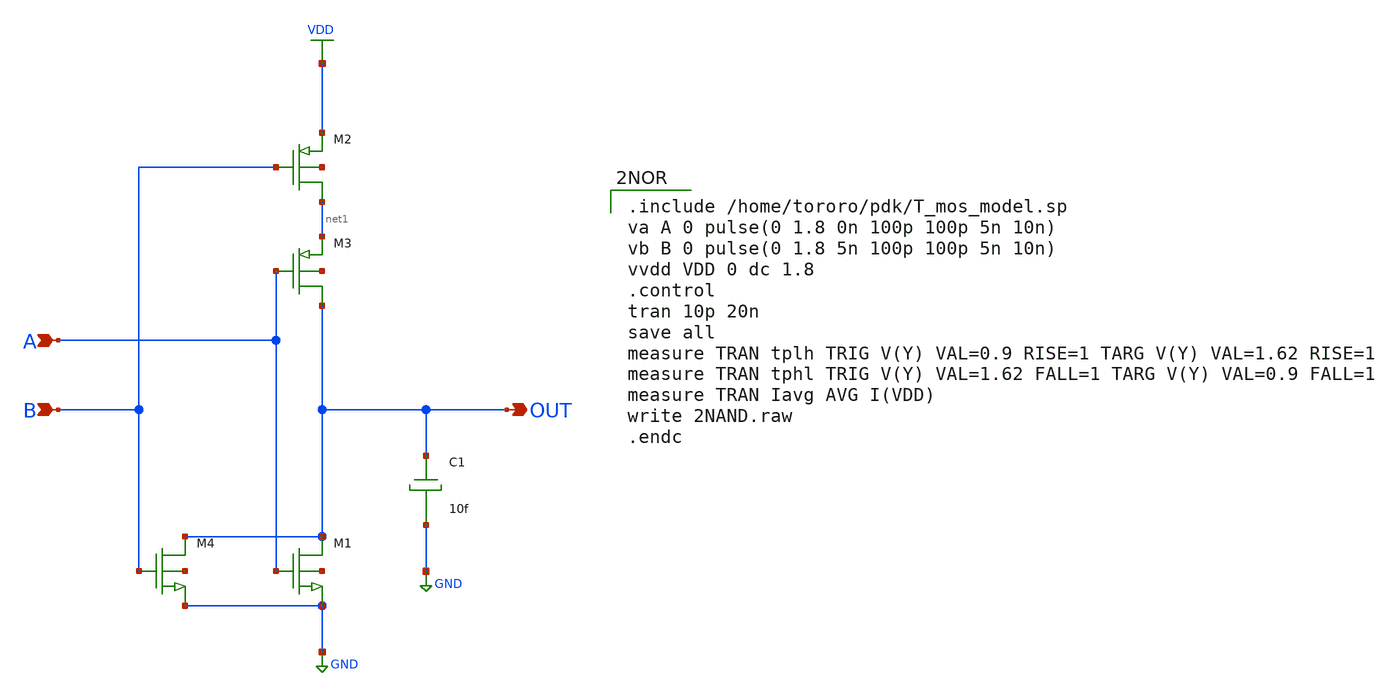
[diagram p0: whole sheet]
** sch_path: outdata/2NOR.sch
**.subckt 2NOR OUT B A
*.opin OUT
*.ipin B
*.ipin A
M1 OUT A GND net2 nch w=9.7u l=1.94u as=0 ps=0 ad=0 pd=0 m=1
M2 net1 B VDD net3 pch w=9.7u l=0.35u as=0 ps=0 ad=0 pd=0 m=1
M3 OUT A net1 net4 pch w=9.7u l=0.35u as=0 ps=0 ad=0 pd=0 m=1
M4 OUT B GND net5 nch w=9.7u l=1.94u as=0 ps=0 ad=0 pd=0 m=1
C1 OUT GND 10f m=1
**** begin user architecture code

.include /home/tororo/pdk/T_mos_model.sp
va A 0 pulse(0 1.8 0n 100p 100p 5n 10n)
vb B 0 pulse(0 1.8 5n 100p 100p 5n 10n)
vvdd VDD 0 dc 1.8
.control
tran 10p 20n
save all
measure TRAN tplh TRIG V(Y) VAL=0.9 RISE=1 TARG V(Y) VAL=1.62 RISE=1
measure TRAN tphl TRIG V(Y) VAL=1.62 FALL=1 TARG V(Y) VAL=0.9 FALL=1
measure TRAN Iavg AVG I(VDD)
write 2NAND.raw
.endc

**** end user architecture code
**.ends
.GLOBAL VDD
.GLOBAL GND
.end
